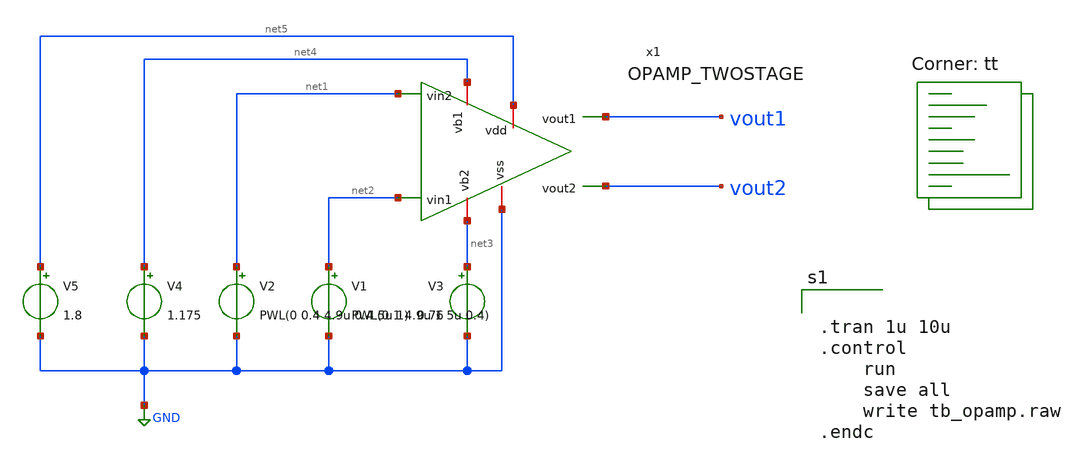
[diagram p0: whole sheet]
** sch_path: TIA/tb_opamp.sch
**.subckt tb_opamp
x1 net5 net4 net1 vout1 net2 vout2 net3 GND OPAMP_TWOSTAGE
V2 net1 GND PWL(0 0.4 4.9u 0.4 5u 1)
V1 net2 GND PWL(0 1 4.9u 1 5u 0.4)
V3 net3 GND 0.76
V4 net4 GND 1.175
V5 net5 GND 1.8
**** begin user architecture code
.lib $::SKYWATER_MODELS/sky130.lib.spice tt


.tran 1u 10u
.control
	run
	save all
	write tb_opamp.raw
.endc


**** end user architecture code
**.ends

* expanding   symbol:  /home/alex/Desktop/EDA/SNN_IPN/TIA/OPAMP_TWOSTAGE.sym # of pins=8
** sym_path: TIA/OPAMP_TWOSTAGE.sym
** sch_path: TIA/OPAMP_TWOSTAGE.sch
.subckt OPAMP_TWOSTAGE vdd vb1 vin2 vout1 vin1 vout2 vb2 vss
*.iopin vb1
*.iopin vb2
*.iopin vss
*.iopin vdd
*.ipin vin1
*.ipin vin2
*.opin vout2
*.opin vout1
XM11 vout1 vx vdd vdd sky130_fd_pr__pfet_01v8 L=0.15 W=25 nf=1 ad='int((nf+1)/2) * W/nf * 0.29' as='int((nf+2)/2) * W/nf * 0.29'
+ pd='2*int((nf+1)/2) * (W/nf + 0.29)' ps='2*int((nf+2)/2) * (W/nf + 0.29)' nrd='0.29 / W' nrs='0.29 / W'
+ sa=0 sb=0 sd=0 mult=1 m=1
XM1 vx vb1 vdd vdd sky130_fd_pr__pfet_01v8 L=0.5 W=1.5 nf=1 ad='int((nf+1)/2) * W/nf * 0.29' as='int((nf+2)/2) * W/nf * 0.29'
+ pd='2*int((nf+1)/2) * (W/nf + 0.29)' ps='2*int((nf+2)/2) * (W/nf + 0.29)' nrd='0.29 / W' nrs='0.29 / W'
+ sa=0 sb=0 sd=0 mult=1 m=1
XM2 vy vb1 vdd vdd sky130_fd_pr__pfet_01v8 L=0.5 W=1.5 nf=1 ad='int((nf+1)/2) * W/nf * 0.29' as='int((nf+2)/2) * W/nf * 0.29'
+ pd='2*int((nf+1)/2) * (W/nf + 0.29)' ps='2*int((nf+2)/2) * (W/nf + 0.29)' nrd='0.29 / W' nrs='0.29 / W'
+ sa=0 sb=0 sd=0 mult=1 m=1
XM3 vout2 vy vdd vdd sky130_fd_pr__pfet_01v8 L=0.15 W=25 nf=1 ad='int((nf+1)/2) * W/nf * 0.29' as='int((nf+2)/2) * W/nf * 0.29'
+ pd='2*int((nf+1)/2) * (W/nf + 0.29)' ps='2*int((nf+2)/2) * (W/nf + 0.29)' nrd='0.29 / W' nrs='0.29 / W'
+ sa=0 sb=0 sd=0 mult=1 m=1
XM4 vx vin1 net1 vss sky130_fd_pr__nfet_01v8 L=0.15 W=0.45 nf=1 ad='int((1 + 1)/2) * 0.45 / 1 * 0.29'
+ as='int((1 + 2)/2) * 0.45 / 1 * 0.29' pd='2*int((1 + 1)/2) * (0.45 / 1 + 0.29)' ps='2*int((1 + 2)/2) * (0.45 / 1 + 0.29)'
+ nrd='0.29 / 0.45 ' nrs='0.29 / 0.45 ' sa=0 sb=0 sd=0 mult=1 m=1
XM5 vy vin2 net1 vss sky130_fd_pr__nfet_01v8 L=0.15 W=0.45 nf=1 ad='int((1 + 1)/2) * 0.45 / 1 * 0.29'
+ as='int((1 + 2)/2) * 0.45 / 1 * 0.29' pd='2*int((1 + 1)/2) * (0.45 / 1 + 0.29)' ps='2*int((1 + 2)/2) * (0.45 / 1 + 0.29)'
+ nrd='0.29 / 0.45 ' nrs='0.29 / 0.45 ' sa=0 sb=0 sd=0 mult=1 m=1
XM6 vout2 vb2 vss vss sky130_fd_pr__nfet_01v8 L=0.15 W=0.87 nf=1 ad='int((1 + 1)/2) * 0.87 / 1 * 0.29'
+ as='int((1 + 2)/2) * 0.87 / 1 * 0.29' pd='2*int((1 + 1)/2) * (0.87 / 1 + 0.29)' ps='2*int((1 + 2)/2) * (0.87 / 1 + 0.29)'
+ nrd='0.29 / 0.87 ' nrs='0.29 / 0.87 ' sa=0 sb=0 sd=0 mult=1 m=1
XM7 vout1 vb2 vss vss sky130_fd_pr__nfet_01v8 L=0.15 W=0.87 nf=1 ad='int((1 + 1)/2) * 0.87 / 1 * 0.29'
+ as='int((1 + 2)/2) * 0.87 / 1 * 0.29' pd='2*int((1 + 1)/2) * (0.87 / 1 + 0.29)' ps='2*int((1 + 2)/2) * (0.87 / 1 + 0.29)'
+ nrd='0.29 / 0.87 ' nrs='0.29 / 0.87 ' sa=0 sb=0 sd=0 mult=1 m=1
XM8 net1 net2 vss vss sky130_fd_pr__nfet_01v8 L=0.15 W=1.45 nf=1 ad='int((1 + 1)/2) * 1.45 / 1 * 0.29'
+ as='int((1 + 2)/2) * 1.45 / 1 * 0.29' pd='2*int((1 + 1)/2) * (1.45 / 1 + 0.29)' ps='2*int((1 + 2)/2) * (1.45 / 1 + 0.29)'
+ nrd='0.29 / 1.45 ' nrs='0.29 / 1.45 ' sa=0 sb=0 sd=0 mult=1 m=1
XM9 net2 net2 vss vss sky130_fd_pr__nfet_01v8 L=0.15 W=18.47 nf=1 ad='int((1 + 1)/2) * 18.47 / 1 * 0.29'
+ as='int((1 + 2)/2) * 18.47 / 1 * 0.29' pd='2*int((1 + 1)/2) * (18.47 / 1 + 0.29)' ps='2*int((1 + 2)/2) * (18.47 / 1 + 0.29)'
+ nrd='0.29 / 18.47 ' nrs='0.29 / 18.47 ' sa=0 sb=0 sd=0 mult=1 m=1
XR4 net2 vdd sky130_fd_pr__res_generic_po W=10 L=207.5 m=1
.ends

.GLOBAL GND
.end
